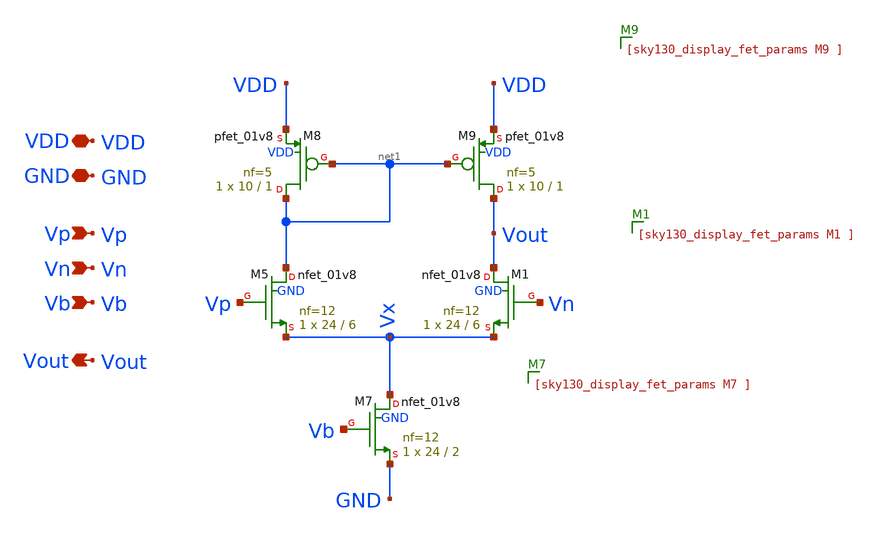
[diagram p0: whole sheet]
** sch_path: sch/archive/old/5t_ota_n.sch
**.subckt 5t_ota_n VDD Vp Vout GND Vn Vb
*.iopin VDD
*.ipin Vp
*.opin Vout
*.iopin GND
*.ipin Vn
*.ipin Vb
XM5 net1 Vp Vx GND sky130_fd_pr__nfet_01v8 L=6 W=24 nf=12 ad='int((12 + 1)/2) * 24 / 12 * 0.29' as='int((12 + 2)/2) * 24 / 12 * 0.29'
+ pd='2*int((12 + 1)/2) * (24 / 12 + 0.29)' ps='2*int((12 + 2)/2) * (24 / 12 + 0.29)' nrd='0.29 / 24 '
+ nrs='0.29 / 24 ' sa=0 sb=0 sd=0 mult=1 m=1
XM7 Vx Vb GND GND sky130_fd_pr__nfet_01v8 L=2 W=24 nf=12 ad='int((12 + 1)/2) * 24 / 12 * 0.29' as='int((12 + 2)/2) * 24 / 12 * 0.29'
+ pd='2*int((12 + 1)/2) * (24 / 12 + 0.29)' ps='2*int((12 + 2)/2) * (24 / 12 + 0.29)' nrd='0.29 / 24 '
+ nrs='0.29 / 24 ' sa=0 sb=0 sd=0 mult=1 m=1
XM8 net1 net1 VDD VDD sky130_fd_pr__pfet_01v8 L=1 W=10 nf=5 ad='int((5 + 1)/2) * 10 / 5 * 0.29' as='int((5 + 2)/2) * 10 / 5 * 0.29'
+ pd='2*int((5 + 1)/2) * (10 / 5 + 0.29)' ps='2*int((5 + 2)/2) * (10 / 5 + 0.29)' nrd='0.29 / 10 ' nrs='0.29 / 10 '
+ sa=0 sb=0 sd=0 mult=1 m=1
XM9 Vout net1 VDD VDD sky130_fd_pr__pfet_01v8 L=1 W=10 nf=5 ad='int((5 + 1)/2) * 10 / 5 * 0.29' as='int((5 + 2)/2) * 10 / 5 * 0.29'
+ pd='2*int((5 + 1)/2) * (10 / 5 + 0.29)' ps='2*int((5 + 2)/2) * (10 / 5 + 0.29)' nrd='0.29 / 10 ' nrs='0.29 / 10 '
+ sa=0 sb=0 sd=0 mult=1 m=1
XM1 Vout Vn Vx GND sky130_fd_pr__nfet_01v8 L=6 W=24 nf=12 ad='int((12 + 1)/2) * 24 / 12 * 0.29' as='int((12 + 2)/2) * 24 / 12 * 0.29'
+ pd='2*int((12 + 1)/2) * (24 / 12 + 0.29)' ps='2*int((12 + 2)/2) * (24 / 12 + 0.29)' nrd='0.29 / 24 '
+ nrs='0.29 / 24 ' sa=0 sb=0 sd=0 mult=1 m=1
**.ends
.end
